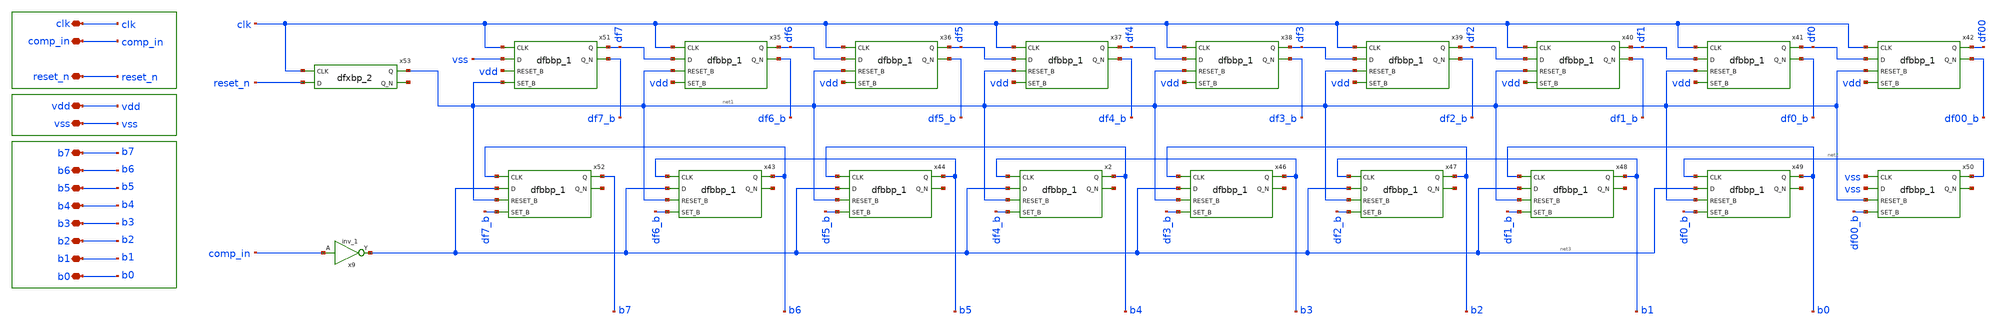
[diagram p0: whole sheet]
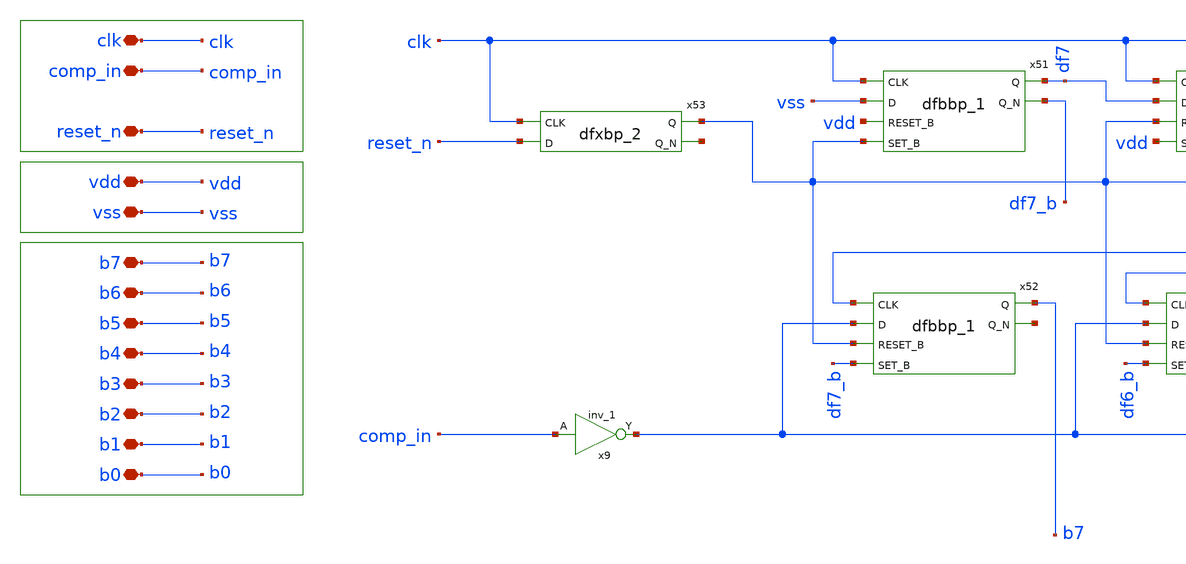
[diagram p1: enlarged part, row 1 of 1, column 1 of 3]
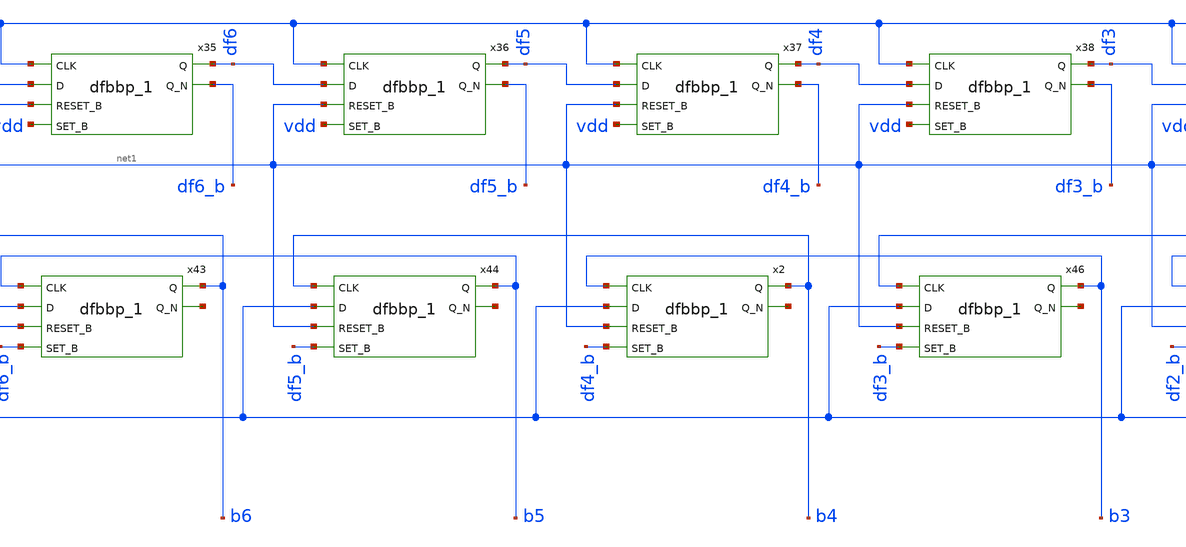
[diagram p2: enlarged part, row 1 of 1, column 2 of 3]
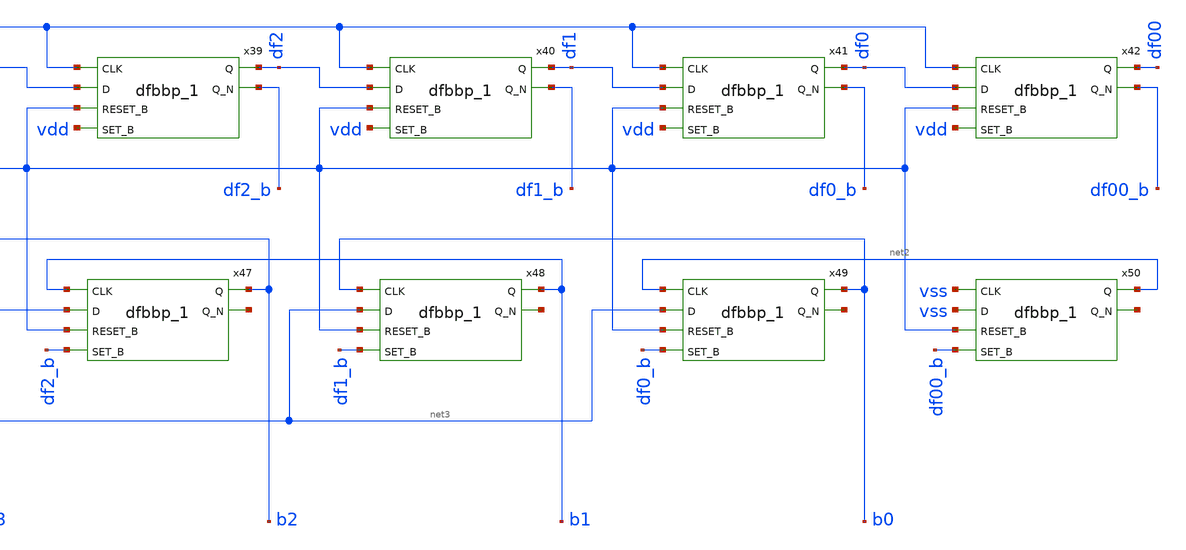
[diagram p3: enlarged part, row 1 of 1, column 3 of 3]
** sch_path: xschem/sar_logic/sarlogic.sch
**.subckt sarlogic vdd clk b7 b6 b5 b4 b3 b2 b1 b0 comp_in vss reset_n
*.iopin vdd
*.iopin clk
*.iopin b7
*.iopin b6
*.iopin b5
*.iopin b4
*.iopin b3
*.iopin b2
*.iopin b1
*.iopin b0
*.iopin comp_in
*.iopin vss
*.iopin reset_n
x35 clk df7 net1 vdd vss vss vdd vdd df6 df6_b sky130_fd_sc_hd__dfbbp_1
x36 clk df6 net1 vdd vss vss vdd vdd df5 df5_b sky130_fd_sc_hd__dfbbp_1
x37 clk df5 net1 vdd vss vss vdd vdd df4 df4_b sky130_fd_sc_hd__dfbbp_1
x38 clk df4 net1 vdd vss vss vdd vdd df3 df3_b sky130_fd_sc_hd__dfbbp_1
x39 clk df3 net1 vdd vss vss vdd vdd df2 df2_b sky130_fd_sc_hd__dfbbp_1
x40 clk df2 net1 vdd vss vss vdd vdd df1 df1_b sky130_fd_sc_hd__dfbbp_1
x41 clk df1 net1 vdd vss vss vdd vdd df0 df0_b sky130_fd_sc_hd__dfbbp_1
x42 clk df0 net1 vdd vss vss vdd vdd df00 df00_b sky130_fd_sc_hd__dfbbp_1
x43 b5 net3 net1 df6_b vss vss vdd vdd b6 net4 sky130_fd_sc_hd__dfbbp_1
x44 b4 net3 net1 df5_b vss vss vdd vdd b5 net5 sky130_fd_sc_hd__dfbbp_1
x2 b3 net3 net1 df4_b vss vss vdd vdd b4 net6 sky130_fd_sc_hd__dfbbp_1
x46 b2 net3 net1 df3_b vss vss vdd vdd b3 net7 sky130_fd_sc_hd__dfbbp_1
x47 b1 net3 net1 df2_b vss vss vdd vdd b2 net8 sky130_fd_sc_hd__dfbbp_1
x48 b0 net3 net1 df1_b vss vss vdd vdd b1 net9 sky130_fd_sc_hd__dfbbp_1
x49 net2 net3 net1 df0_b vss vss vdd vdd b0 net10 sky130_fd_sc_hd__dfbbp_1
x50 vss vss net1 df00_b vss vss vdd vdd net2 net11 sky130_fd_sc_hd__dfbbp_1
x51 clk vss vdd net1 vss vss vdd vdd df7 df7_b sky130_fd_sc_hd__dfbbp_1
x52 b6 net3 net1 df7_b vss vss vdd vdd b7 net12 sky130_fd_sc_hd__dfbbp_1
x53 clk reset_n vss vss vdd vdd net1 net13 sky130_fd_sc_hd__dfxbp_2
x9 comp_in vss vss vdd vdd net3 sky130_fd_sc_hd__inv_1
**.ends
.end
